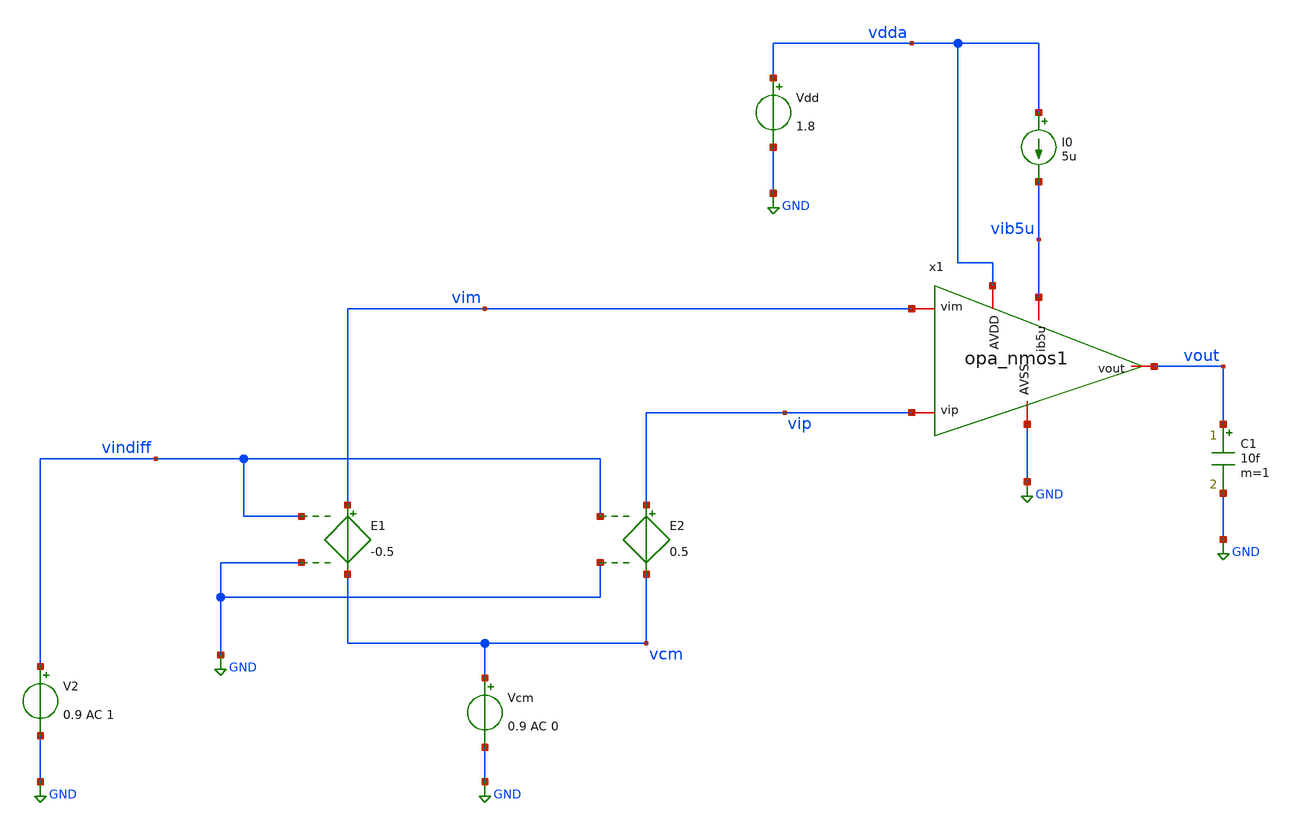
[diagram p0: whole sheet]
** sch_path: xschem/TB_opa_nmos.sch
**.subckt TB_opa_nmos
E2 vip vcm vindiff GND 0.5
E1 vim vcm vindiff GND -0.5
x1 vout vip GND vim vdda vib5u opa_nmos1
Vcm vcm GND 0.9 AC 0
V2 vindiff GND 0.9 AC 1
C1 vout GND 10f m=1
Vdd vdda GND 1.8
I0 vdda vib5u 5u
**** begin user architecture code

** opencircuitdesign pdks install
.lib $::SKYWATER_MODELS/sky130.lib.spice tt




* ngspice commands
.temp 27
.control

 save all

 save @m.x1.xm1.msky130_fd_pr__nfet_01v8[id]
 save @m.x1.xm1.msky130_fd_pr__nfet_01v8[gm]

 save @m.x1.xmim.msky130_fd_pr__nfet_01v8_lvt[id]
 save @m.x1.xmim.msky130_fd_pr__nfet_01v8_lvt[gm]

 save @m.x1.xmip.msky130_fd_pr__nfet_01v8_lvt[id]
 save @m.x1.xmip.msky130_fd_pr__nfet_01v8_lvt[gm]

 save @m.x1.xmpcmm.msky130_fd_pr__pfet_01v8_lvt[id]
 save @m.x1.xmpcmm.msky130_fd_pr__pfet_01v8_lvt[gm]

 save @m.x1.xmpcmp.msky130_fd_pr__pfet_01v8_lvt[id]
 save @m.x1.xmpcmp.msky130_fd_pr__pfet_01v8_lvt[gm]

 save @m.x1.xmtail.msky130_fd_pr__nfet_01v8[id]
 save @m.x1.xmtail.msky130_fd_pr__nfet_01v8[gm]

 OP

 write TB_opa_nmos1.raw

 let im1=@m.x1.xm1.msky130_fd_pr__nfet_01v8[id]
 let iim=@m.x1.xmim.msky130_fd_pr__nfet_01v8_lvt[id]
 let iip=@m.x1.xmip.msky130_fd_pr__nfet_01v8_lvt[id]
 let icmm=@m.x1.xmpcmm.msky130_fd_pr__pfet_01v8_lvt[id]
 let icmp=@m.x1.xmpcmp.msky130_fd_pr__pfet_01v8_lvt[id]
 let imtail=@m.x1.xmtail.msky130_fd_pr__nfet_01v8[id]

 let gm1=@m.x1.xm1.msky130_fd_pr__nfet_01v8[gm]
 let gmim=@m.x1.xmim.msky130_fd_pr__nfet_01v8_lvt[gm]
 let gmip=@m.x1.xmip.msky130_fd_pr__nfet_01v8_lvt[gm]
 let gmcmm=@m.x1.xmpcmm.msky130_fd_pr__pfet_01v8_lvt[gm]
 let gmcmp=@m.x1.xmpcmp.msky130_fd_pr__pfet_01v8_lvt[gm]
 let gmtail=@m.x1.xmtail.msky130_fd_pr__nfet_01v8[gm]

 let gmidm1=gm1/im1
 let gmidim=gmim/iim
 let gmidip=gmip/iip
 let gmidcmm=gmcmm/icmm
 let gmidcmp=gmcmp/icmp
 let gmidtail=gmtail/imtail

 print gmidm1
 print gmidim
 print gmidip
 print gmidcmm
 print gmidcmp
 print gmidtail

 print im1
 print iim
 print iip
 print icmm
 print icmp
 print imtail

 AC DEC 100 1 1e9
**plot v(vout)
**plot vdb(vout)
 set appendwrite
 write TB_opa_nmos1.raw

.endc
.end




**** end user architecture code
**.ends

* expanding   symbol:  opa_nmos1.sym # of pins=6
** sym_path: xschem/opa_nmos1.sym
** sch_path: xschem/opa_nmos1.sch
.subckt opa_nmos1 vout vip AVSS vim AVDD ib5u
*.iopin vip
*.iopin vim
*.iopin vout
*.iopin ib5u
*.iopin AVDD
*.iopin AVSS
XM1 ib5u ib5u AVSS AVSS sky130_fd_pr__nfet_01v8 L=1 W=5 nf=1 ad='int((1 + 1)/2) * 5 / 1 * 0.29' as='int((1 + 2)/2) * 5 / 1 * 0.29'
+ pd='2*int((1 + 1)/2) * (5 / 1 + 0.29)' ps='2*int((1 + 2)/2) * (5 / 1 + 0.29)' nrd='0.29 / 5 ' nrs='0.29 / 5 '
+ sa=0 sb=0 sd=0 mult=1 m=1
XM2 net1 ib5u AVSS AVSS sky130_fd_pr__nfet_01v8 L=1 W=5 nf=1 ad='int((1 + 1)/2) * 5 / 1 * 0.29' as='int((1 + 2)/2) * 5 / 1 * 0.29'
+ pd='2*int((1 + 1)/2) * (5 / 1 + 0.29)' ps='2*int((1 + 2)/2) * (5 / 1 + 0.29)' nrd='0.29 / 5 ' nrs='0.29 / 5 '
+ sa=0 sb=0 sd=0 mult=2 m=2
XM3 vom vip net1 net1 sky130_fd_pr__nfet_01v8_lvt L=2 W=5 nf=1 ad='int((1 + 1)/2) * 5 / 1 * 0.29' as='int((1 + 2)/2) * 5 / 1 * 0.29'
+ pd='2*int((1 + 1)/2) * (5 / 1 + 0.29)' ps='2*int((1 + 2)/2) * (5 / 1 + 0.29)' nrd='0.29 / 5 ' nrs='0.29 / 5 '
+ sa=0 sb=0 sd=0 mult=4 m=4
XM4 vout vim net1 net1 sky130_fd_pr__nfet_01v8_lvt L=2 W=4 nf=1 ad='int((1 + 1)/2) * 4 / 1 * 0.29' as='int((1 + 2)/2) * 4 / 1 * 0.29'
+ pd='2*int((1 + 1)/2) * (4 / 1 + 0.29)' ps='2*int((1 + 2)/2) * (4 / 1 + 0.29)' nrd='0.29 / 4 ' nrs='0.29 / 4 '
+ sa=0 sb=0 sd=0 mult=5 m=5
XM11 vom vom AVDD AVDD sky130_fd_pr__pfet_01v8 L=2 W=5 nf=1 ad='int((nf+1)/2) * W/nf * 0.29' as='int((nf+2)/2) * W/nf * 0.29'
+ pd='2*int((nf+1)/2) * (W/nf + 0.29)' ps='2*int((nf+2)/2) * (W/nf + 0.29)' nrd='0.29 / W' nrs='0.29 / W'
+ sa=0 sb=0 sd=0 mult=2 m=2
XM5 vout vom AVDD AVDD sky130_fd_pr__pfet_01v8 L=2 W=5 nf=1 ad='int((nf+1)/2) * W/nf * 0.29' as='int((nf+2)/2) * W/nf * 0.29'
+ pd='2*int((nf+1)/2) * (W/nf + 0.29)' ps='2*int((nf+2)/2) * (W/nf + 0.29)' nrd='0.29 / W' nrs='0.29 / W'
+ sa=0 sb=0 sd=0 mult=2 m=2
**** begin user architecture code



* ngspice commands




**** end user architecture code
.ends

.GLOBAL GND
.end
